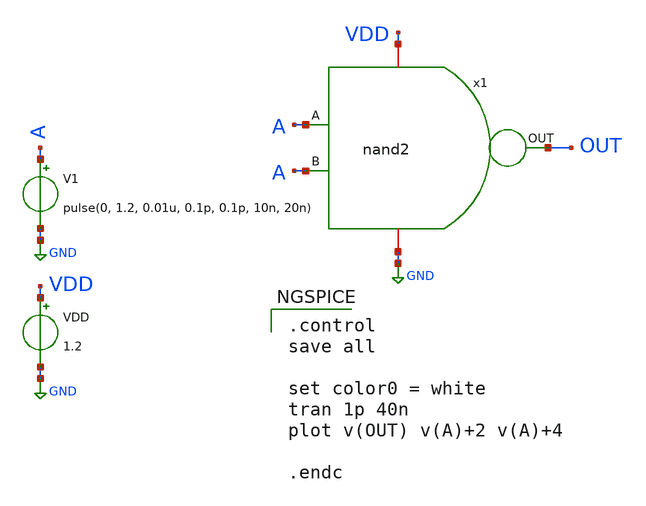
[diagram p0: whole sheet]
** sch_path: design/ALU/nand2_tb.sch
**.subckt nand2_tb
VDD VDD GND 1.2
V1 A GND pulse(0, 1.2, 0.01u, 0.1p, 0.1p, 10n, 20n)
x1 VDD OUT A A GND nand2
**** begin user architecture code

** opencircuitdesign pdks install
.lib $::SKYWATER_MODELS/sky130.lib.spice tt_mm



.control
save all

set color0 = white
tran 1p 40n
plot v(OUT) v(A)+2 v(A)+4

.endc

**** end user architecture code
**.ends
.GLOBAL GND
.end
